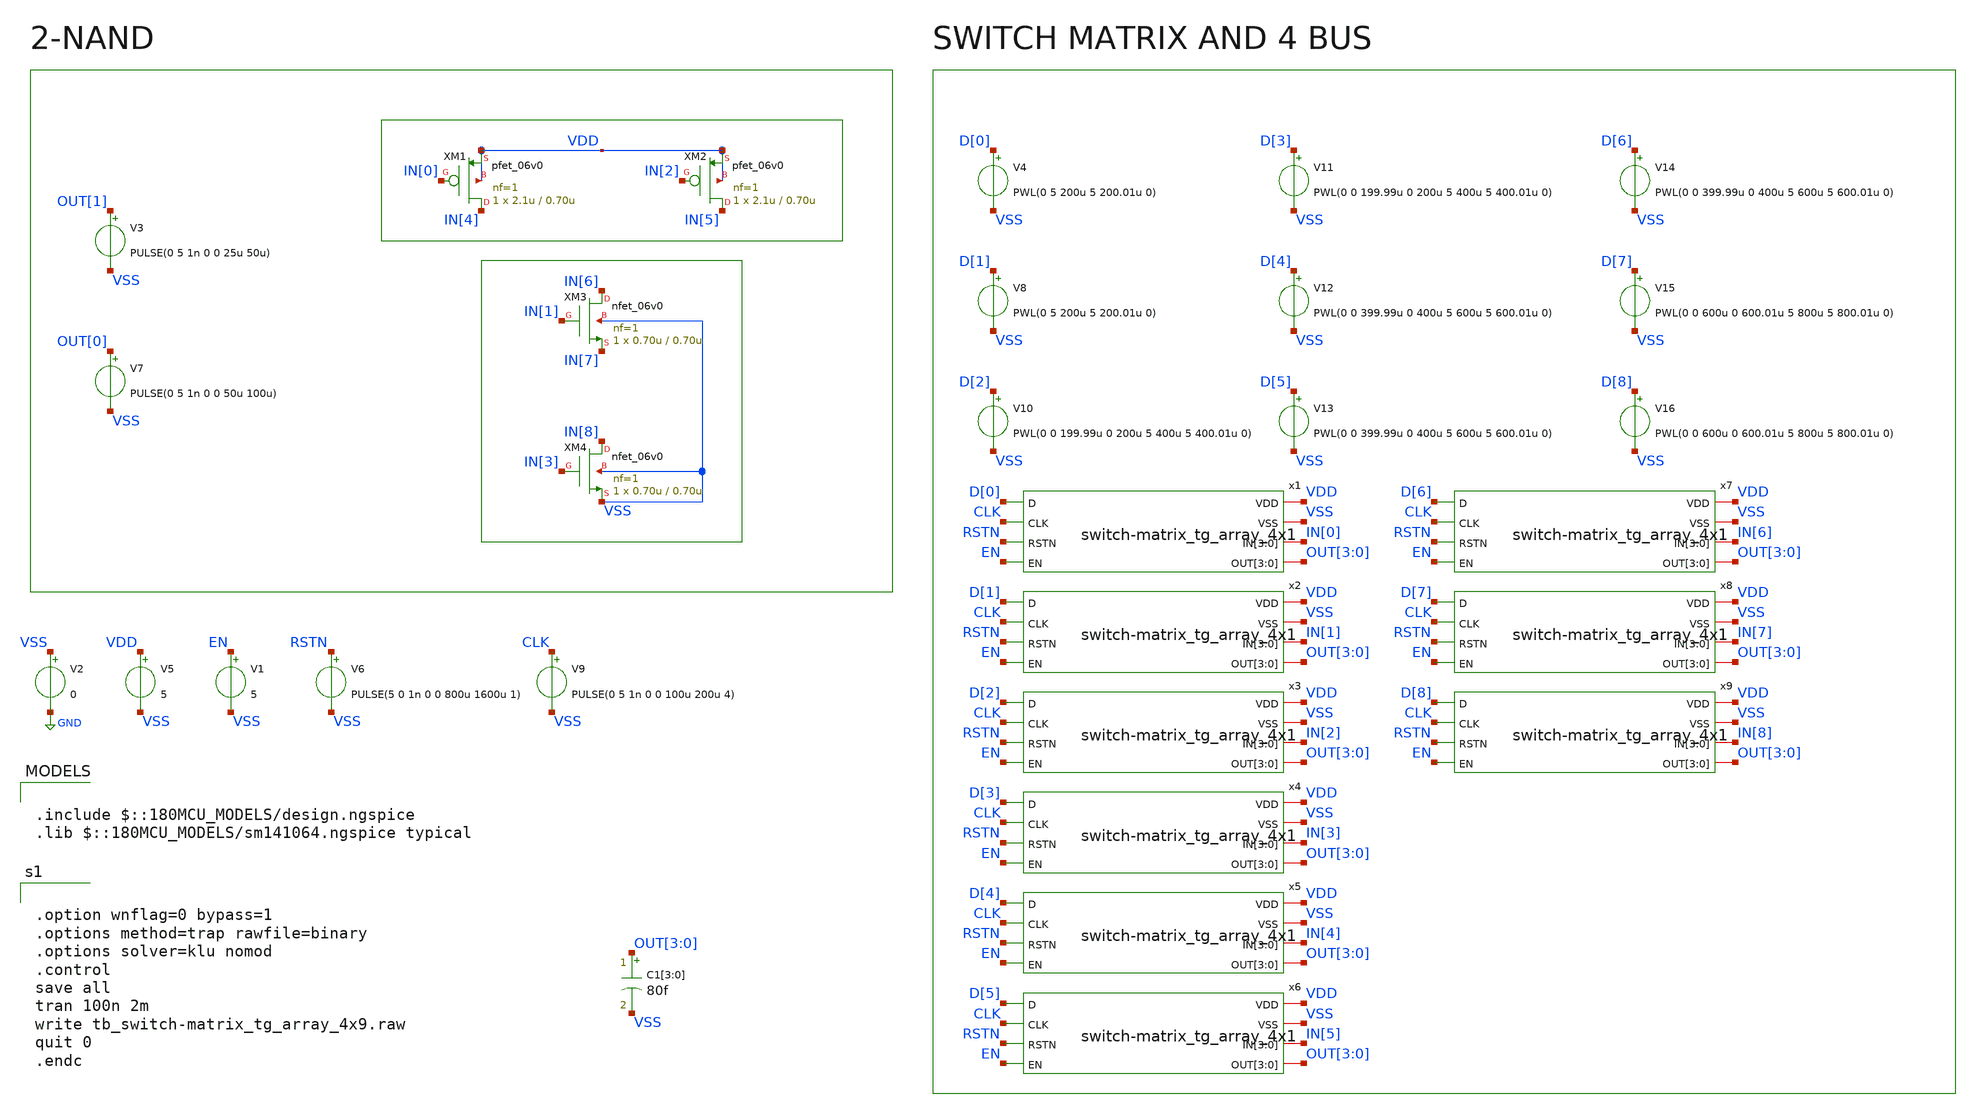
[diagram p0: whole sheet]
** sch_path: designs/libs/core_switch-matrix/tb_switch-matrix/tb_switch-matrix_tg_array_4x9.sch
**.subckt tb_switch-matrix_tg_array_4x9
V2 VSS GND 0
V3 OUT[1] VSS PULSE(0 5 1n 0 0 25u 50u)
V4 D[0] VSS PWL(0 5 200u 5 200.01u 0)
V5 VDD VSS 5
V9 CLK VSS PULSE(0 5 1n 0 0 100u 200u 4)
V1 EN VSS 5
V6 RSTN VSS PULSE(5 0 1n 0 0 800u 1600u 1)
V7 OUT[0] VSS PULSE(0 5 1n 0 0 50u 100u)
V8 D[1] VSS PWL(0 5 200u 5 200.01u 0)
V10 D[2] VSS PWL(0 0 199.99u 0 200u 5 400u 5 400.01u 0)
V11 D[3] VSS PWL(0 0 199.99u 0 200u 5 400u 5 400.01u 0)
V12 D[4] VSS PWL(0 0 399.99u 0 400u 5 600u 5 600.01u 0)
V13 D[5] VSS PWL(0 0 399.99u 0 400u 5 600u 5 600.01u 0)
C1[3] OUT[3] VSS 80f m=1
C1[2] OUT[2] VSS 80f m=1
C1[1] OUT[1] VSS 80f m=1
C1[0] OUT[0] VSS 80f m=1
XM1 IN[4] IN[0] VDD VDD pfet_06v0 L=0.70u W=2.1u nf=1 ad='int((nf+1)/2) * W/nf * 0.18u' as='int((nf+2)/2) * W/nf * 0.18u'
+ pd='2*int((nf+1)/2) * (W/nf + 0.18u)' ps='2*int((nf+2)/2) * (W/nf + 0.18u)' nrd='0.18u / W' nrs='0.18u / W'
+ sa=0 sb=0 sd=0 m=1
XM2 IN[5] IN[2] VDD VDD pfet_06v0 L=0.70u W=2.1u nf=1 ad='int((nf+1)/2) * W/nf * 0.18u' as='int((nf+2)/2) * W/nf * 0.18u'
+ pd='2*int((nf+1)/2) * (W/nf + 0.18u)' ps='2*int((nf+2)/2) * (W/nf + 0.18u)' nrd='0.18u / W' nrs='0.18u / W'
+ sa=0 sb=0 sd=0 m=1
XM3 IN[6] IN[1] IN[7] VSS nfet_06v0 L=0.70u W=0.70u nf=1 ad='int((nf+1)/2) * W/nf * 0.18u' as='int((nf+2)/2) * W/nf * 0.18u'
+ pd='2*int((nf+1)/2) * (W/nf + 0.18u)' ps='2*int((nf+2)/2) * (W/nf + 0.18u)' nrd='0.18u / W' nrs='0.18u / W'
+ sa=0 sb=0 sd=0 m=1
XM4 IN[8] IN[3] VSS VSS nfet_06v0 L=0.70u W=0.70u nf=1 ad='int((nf+1)/2) * W/nf * 0.18u' as='int((nf+2)/2) * W/nf * 0.18u'
+ pd='2*int((nf+1)/2) * (W/nf + 0.18u)' ps='2*int((nf+2)/2) * (W/nf + 0.18u)' nrd='0.18u / W' nrs='0.18u / W'
+ sa=0 sb=0 sd=0 m=1
V14 D[6] VSS PWL(0 0 399.99u 0 400u 5 600u 5 600.01u 0)
V15 D[7] VSS PWL(0 0 600u 0 600.01u 5 800u 5 800.01u 0)
V16 D[8] VSS PWL(0 0 600u 0 600.01u 5 800u 5 800.01u 0)
x1 VDD VSS IN[0] IN[0] IN[0] IN[0] OUT[3] OUT[2] OUT[1] OUT[0] D[0] CLK RSTN EN
+ switch-matrix_tg_array_4x1
x2 VDD VSS IN[1] IN[1] IN[1] IN[1] OUT[3] OUT[2] OUT[1] OUT[0] D[1] CLK RSTN EN
+ switch-matrix_tg_array_4x1
x3 VDD VSS IN[2] IN[2] IN[2] IN[2] OUT[3] OUT[2] OUT[1] OUT[0] D[2] CLK RSTN EN
+ switch-matrix_tg_array_4x1
x4 VDD VSS IN[3] IN[3] IN[3] IN[3] OUT[3] OUT[2] OUT[1] OUT[0] D[3] CLK RSTN EN
+ switch-matrix_tg_array_4x1
x5 VDD VSS IN[4] IN[4] IN[4] IN[4] OUT[3] OUT[2] OUT[1] OUT[0] D[4] CLK RSTN EN
+ switch-matrix_tg_array_4x1
x6 VDD VSS IN[5] IN[5] IN[5] IN[5] OUT[3] OUT[2] OUT[1] OUT[0] D[5] CLK RSTN EN
+ switch-matrix_tg_array_4x1
x7 VDD VSS IN[6] IN[6] IN[6] IN[6] OUT[3] OUT[2] OUT[1] OUT[0] D[6] CLK RSTN EN
+ switch-matrix_tg_array_4x1
x8 VDD VSS IN[7] IN[7] IN[7] IN[7] OUT[3] OUT[2] OUT[1] OUT[0] D[7] CLK RSTN EN
+ switch-matrix_tg_array_4x1
x9 VDD VSS IN[8] IN[8] IN[8] IN[8] OUT[3] OUT[2] OUT[1] OUT[0] D[8] CLK RSTN EN
+ switch-matrix_tg_array_4x1
**** begin user architecture code

.include $::180MCU_MODELS/design.ngspice
.lib $::180MCU_MODELS/sm141064.ngspice typical



.option wnflag=0 bypass=1
.options method=trap rawfile=binary
.options solver=klu nomod
.control
save all
tran 100n 2m
write tb_switch-matrix_tg_array_4x9.raw
quit 0
.endc


**** end user architecture code
**.ends
.GLOBAL GND
.end
